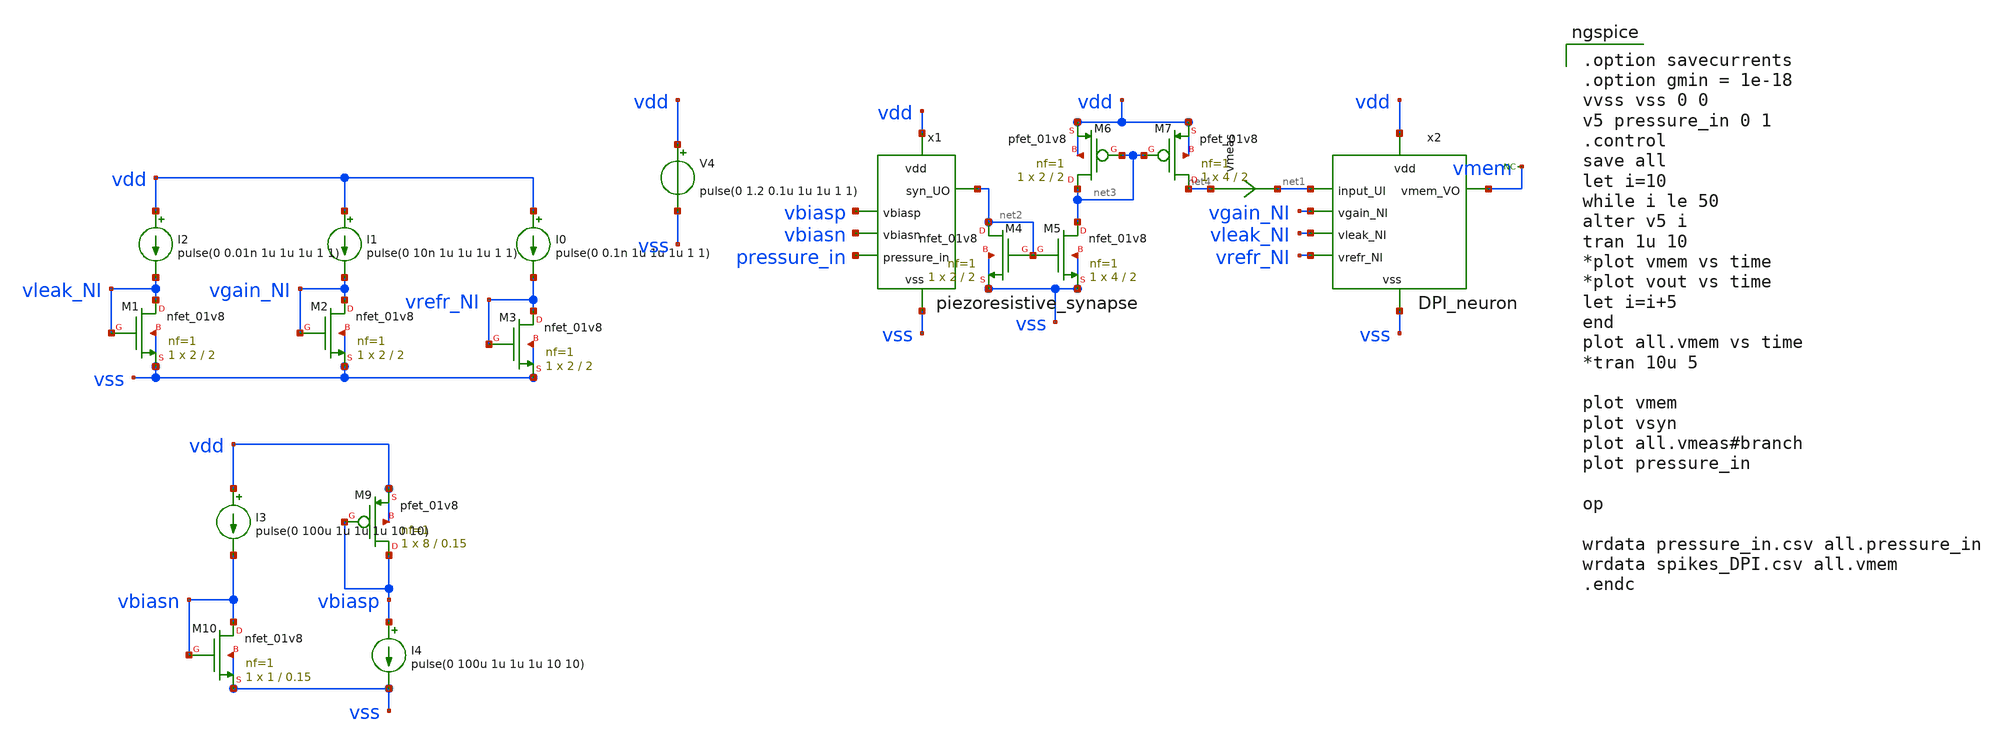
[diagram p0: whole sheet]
** sch_path: circuits/DPI_and_piezo.sch
* Copyright 2020 Stefan Frederik Schippers
* Licensed under the Apache License, Version 2.0 (the "License");
* you may not use this file except in compliance with the License.
* You may obtain a copy of the License at
* https://www.apache.org/licenses/LICENSE-2.0
* Unless required by applicable law or agreed to in writing, software
* distributed under the License is distributed on an "AS IS" BASIS,
* WITHOUT WARRANTIES OR CONDITIONS OF ANY KIND, either express or implied.
* See the License for the specific language governing permissions and
* limitations under the License.
**.subckt DPI_and_piezo
x2 net1 vdd vgain_NI vleak_NI vrefr_NI vss vmem DPI_neuron
I0 vdd vrefr_NI pulse(0 0.1n 1u 1u 1u 1 1)
I1 vdd vgain_NI pulse(0 10n 1u 1u 1u 1 1)
I2 vdd vleak_NI pulse(0 0.01n 1u 1u 1u 1 1)
XM1 vleak_NI vleak_NI vss vss sky130_fd_pr__nfet_01v8 L=2 W=2 nf=1 ad='int((nf+1)/2) * W/nf * 0.29' as='int((nf+2)/2) * W/nf * 0.29'
+ pd='2*int((nf+1)/2) * (W/nf + 0.29)' ps='2*int((nf+2)/2) * (W/nf + 0.29)' nrd='0.29 / W' nrs='0.29 / W'
+ sa=0 sb=0 sd=0 mult=1 m=1
XM2 vgain_NI vgain_NI vss vss sky130_fd_pr__nfet_01v8 L=2 W=2 nf=1 ad='int((nf+1)/2) * W/nf * 0.29' as='int((nf+2)/2) * W/nf * 0.29'
+ pd='2*int((nf+1)/2) * (W/nf + 0.29)' ps='2*int((nf+2)/2) * (W/nf + 0.29)' nrd='0.29 / W' nrs='0.29 / W'
+ sa=0 sb=0 sd=0 mult=1 m=1
XM3 vrefr_NI vrefr_NI vss vss sky130_fd_pr__nfet_01v8 L=2 W=2 nf=1 ad='int((nf+1)/2) * W/nf * 0.29' as='int((nf+2)/2) * W/nf * 0.29'
+ pd='2*int((nf+1)/2) * (W/nf + 0.29)' ps='2*int((nf+2)/2) * (W/nf + 0.29)' nrd='0.29 / W' nrs='0.29 / W'
+ sa=0 sb=0 sd=0 mult=1 m=1
V4 vdd vss pulse(0 1.2 0.1u 1u 1u 1 1)
x1 vdd vbiasp vbiasn pressure_in vss net2 piezoresistive_synapse
vmeas net4 net1 0
.save i(vmeas)
* noconn vmem
XM9 vbiasp vbiasp vdd vdd sky130_fd_pr__pfet_01v8 L=0.15 W=8 nf=1 ad='int((nf+1)/2) * W/nf * 0.29' as='int((nf+2)/2) * W/nf * 0.29'
+ pd='2*int((nf+1)/2) * (W/nf + 0.29)' ps='2*int((nf+2)/2) * (W/nf + 0.29)' nrd='0.29 / W' nrs='0.29 / W'
+ sa=0 sb=0 sd=0 mult=1 m=1
XM10 vbiasn vbiasn vss vss sky130_fd_pr__nfet_01v8 L=0.15 W=1 nf=1 ad='int((nf+1)/2) * W/nf * 0.29' as='int((nf+2)/2) * W/nf * 0.29'
+ pd='2*int((nf+1)/2) * (W/nf + 0.29)' ps='2*int((nf+2)/2) * (W/nf + 0.29)' nrd='0.29 / W' nrs='0.29 / W'
+ sa=0 sb=0 sd=0 mult=1 m=1
I3 vdd vbiasn pulse(0 100u 1u 1u 1u 10 10)
I4 vbiasp vss pulse(0 100u 1u 1u 1u 10 10)
XM4 net2 net2 vss vss sky130_fd_pr__nfet_01v8 L=2 W=2 nf=1 ad='int((nf+1)/2) * W/nf * 0.29' as='int((nf+2)/2) * W/nf * 0.29'
+ pd='2*int((nf+1)/2) * (W/nf + 0.29)' ps='2*int((nf+2)/2) * (W/nf + 0.29)' nrd='0.29 / W' nrs='0.29 / W'
+ sa=0 sb=0 sd=0 mult=1 m=1
XM5 net3 net2 vss vss sky130_fd_pr__nfet_01v8 L=2 W=4 nf=1 ad='int((nf+1)/2) * W/nf * 0.29' as='int((nf+2)/2) * W/nf * 0.29'
+ pd='2*int((nf+1)/2) * (W/nf + 0.29)' ps='2*int((nf+2)/2) * (W/nf + 0.29)' nrd='0.29 / W' nrs='0.29 / W'
+ sa=0 sb=0 sd=0 mult=1 m=1
XM6 net3 net3 vdd vdd sky130_fd_pr__pfet_01v8 L=2 W=2 nf=1 ad='int((nf+1)/2) * W/nf * 0.29' as='int((nf+2)/2) * W/nf * 0.29'
+ pd='2*int((nf+1)/2) * (W/nf + 0.29)' ps='2*int((nf+2)/2) * (W/nf + 0.29)' nrd='0.29 / W' nrs='0.29 / W'
+ sa=0 sb=0 sd=0 mult=1 m=1
XM7 net4 net3 vdd vdd sky130_fd_pr__pfet_01v8 L=2 W=4 nf=1 ad='int((nf+1)/2) * W/nf * 0.29' as='int((nf+2)/2) * W/nf * 0.29'
+ pd='2*int((nf+1)/2) * (W/nf + 0.29)' ps='2*int((nf+2)/2) * (W/nf + 0.29)' nrd='0.29 / W' nrs='0.29 / W'
+ sa=0 sb=0 sd=0 mult=1 m=1
**** begin user architecture code

.option savecurrents
.option gmin = 1e-18
vvss vss 0 0
v5 pressure_in 0 1
.control
save all
let i=10
while i le 50
alter v5 i
tran 1u 10
*plot vmem vs time
*plot vout vs time
let i=i+5
end
plot all.vmem vs time
*tran 10u 5

plot vmem
plot vsyn
plot all.vmeas#branch
plot pressure_in

op

wrdata pressure_in.csv all.pressure_in
wrdata spikes_DPI.csv all.vmem
.endc


 .lib $::SKYWATER_MODELS/models/sky130.lib.spice tt

.param mc_mm_switch=0
.param mc_pr_switch=1


**** end user architecture code
**.ends
.end
